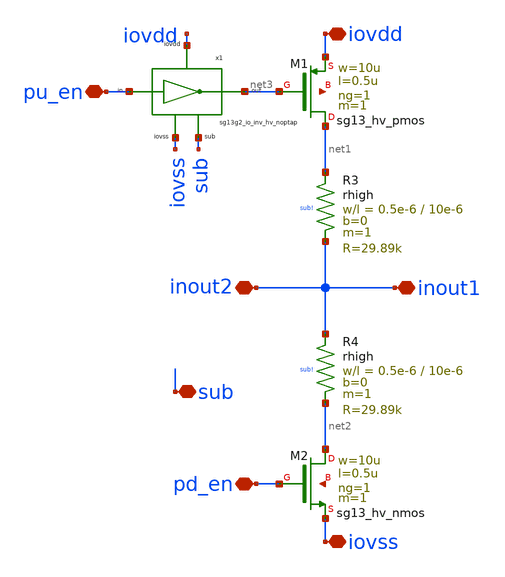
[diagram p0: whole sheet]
** sch_path: libs.tech/xschem/hm_stdcells/hm_PUPD_noptap.sch
**.subckt hm_PUPD_noptap inout1 pu_en pd_en iovdd inout2 iovss sub
*.iopin inout1
*.iopin pu_en
*.iopin pd_en
*.iopin iovdd
*.iopin inout2
*.iopin iovss
*.iopin sub
XR3 net1 inout1 sub! rhigh w=0.5e-6 l=10e-6 m=1 b=0 mm_ok=1
XR4 inout1 net2 sub! rhigh w=0.5e-6 l=10e-6 m=1 b=0 mm_ok=1
XM1 net1 net3 iovdd net4 sg13_hv_pmos w=10u l=0.5u ng=1 m=1 mm_ok=1
XM2 net2 pd_en iovss net5 sg13_hv_nmos w=10u l=0.5u ng=1 m=1 mm_ok=1
x1 iovdd net3 pu_en iovss sub sg13g2_io_inv_hv_noptap
**.ends

* expanding   symbol:
*+  /home/designer/shared/hm-openpdk-library/libs.tech/xschem/hm_stdcells/sg13g2_io_inv_hv_noptap.sym # of pins=5
** sym_path: libs.tech/xschem/hm_stdcells/sg13g2_io_inv_hv_noptap.sym
** sch_path: libs.tech/xschem/hm_stdcells/sg13g2_io_inv_hv_noptap.sch
.subckt sg13g2_io_inv_hv_noptap iovdd out in iovss sub
*.iopin out
*.iopin iovdd
*.iopin iovss
*.iopin sub
*.iopin in
XM1 out in iovdd net1 sg13_hv_pmos w=10u l=0.5u ng=1 m=1 mm_ok=1
XM2 out in iovss net2 sg13_hv_nmos w=10u l=0.5u ng=1 m=1 mm_ok=1
.ends

.end
